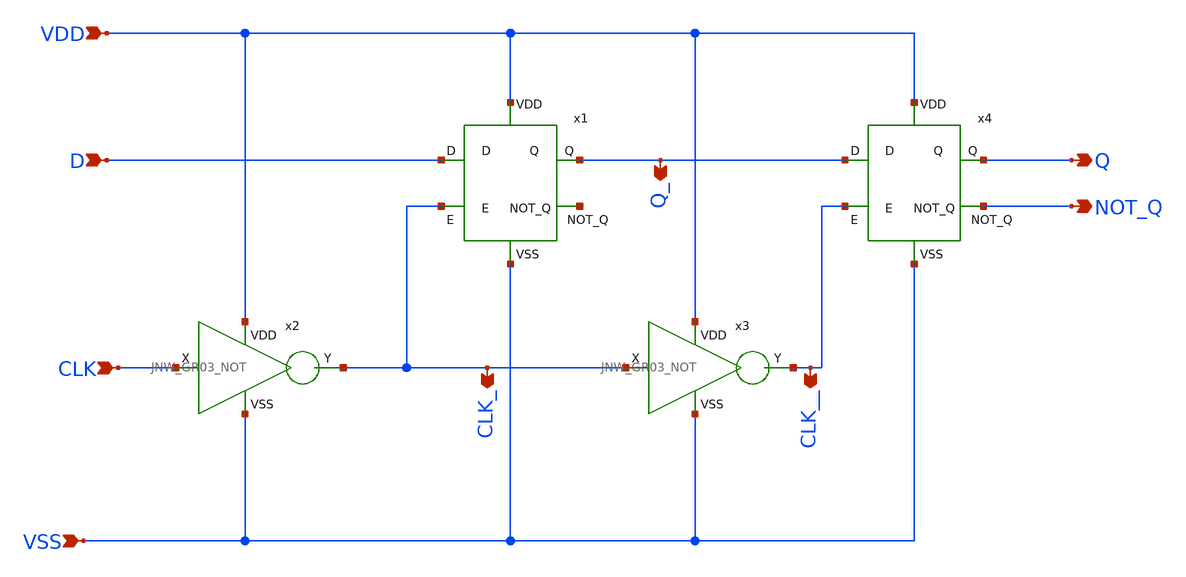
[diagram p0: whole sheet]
** sch_path: design/JNW_GR03_SKY130A/JNW_GR03_DFLIPFLOP_R.sch
**.subckt JNW_GR03_DFLIPFLOP_R VDD VSS D CLK Q NOT_Q CLK_ CLK__ Q_
*.ipin VDD
*.ipin VSS
*.ipin D
*.ipin CLK
*.opin Q
*.opin NOT_Q
*.opin CLK_
*.opin CLK__
*.opin Q_
x1 VDD D Q_ net1 CLK_ VSS JNW_GR03_DLATCH
x2 VDD CLK CLK_ VSS JNW_GR03_NOT
x3 VDD CLK_ CLK__ VSS JNW_GR03_NOT
x4 VDD Q_ Q NOT_Q CLK__ VSS JNW_GR03_DLATCH
**.ends
.end
